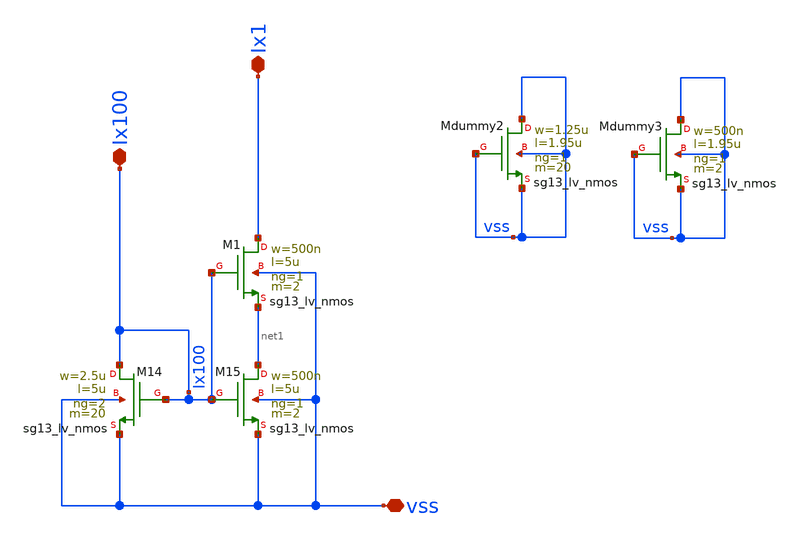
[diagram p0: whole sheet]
** sch_path: v2_feature_extr_withf/current_mirror_100x.sch
**.subckt current_mirror_100x Ix100 Ix1 vss
*.iopin Ix100
*.iopin Ix1
*.iopin vss
XM14 Ix100 Ix100 vss vss sg13_lv_nmos w=2.5u l=5u ng=2 m=20 mm_ok=1
XM15 net1 Ix100 vss vss sg13_lv_nmos w=500n l=5u ng=1 m=2 mm_ok=1
XM1 Ix1 Ix100 net1 vss sg13_lv_nmos w=500n l=5u ng=1 m=2 mm_ok=1
XMdummy2 vss vss vss vss sg13_lv_nmos w=1.25u l=1.95u ng=1 m=20 mm_ok=1
XMdummy3 vss vss vss vss sg13_lv_nmos w=500n l=1.95u ng=1 m=2 mm_ok=1
**.ends
.end
